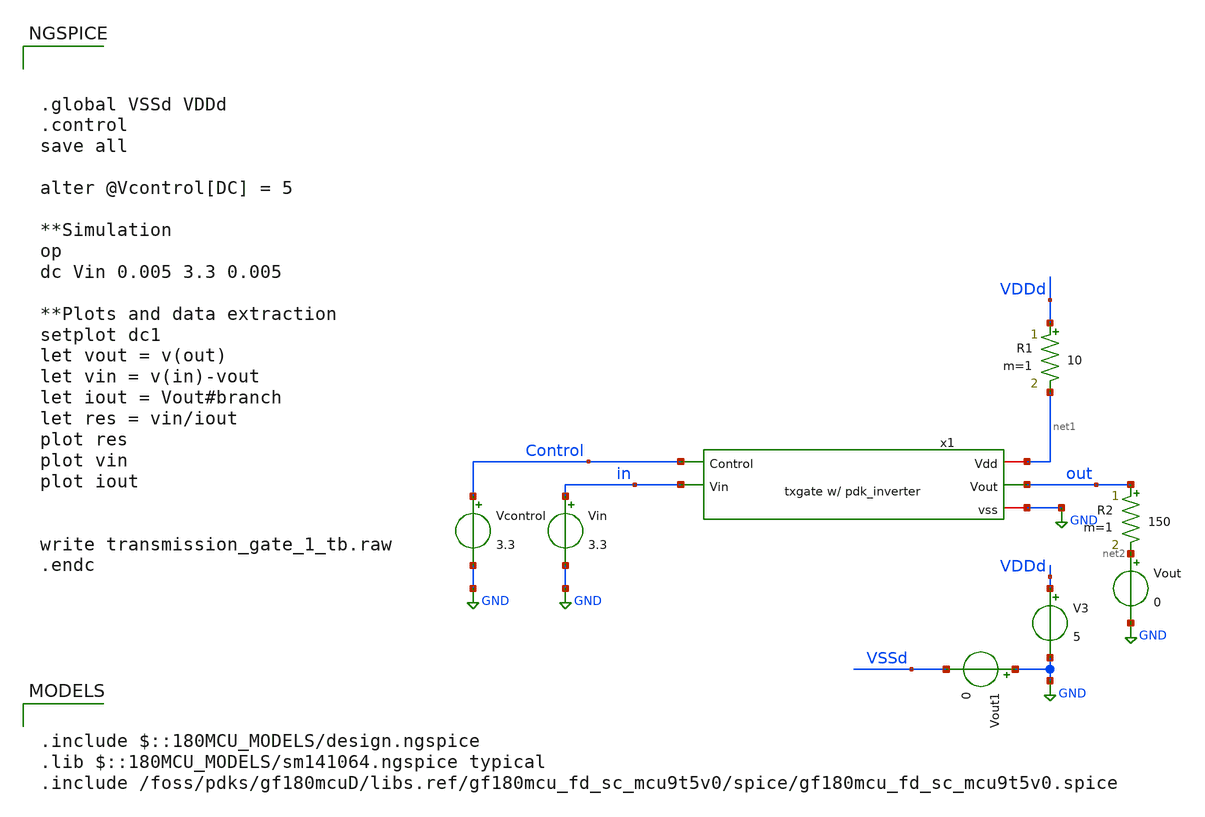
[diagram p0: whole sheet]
** sch_path: designs/libs/tb_analog/tb_txgate/transmission_gate_1_tb.sch
**.subckt transmission_gate_1_tb
Vin in GND 3.3
Vcontrol Control GND 3.3
V3 VDDd GND 5
Vout net2 GND 0
R1 VDDd net1 10 m=1
x1 net1 Control out in GND transmission_gate_2
Vout1 GND VSSd 0
R2 out net2 150 m=1
**** begin user architecture code

.include $::180MCU_MODELS/design.ngspice
.lib $::180MCU_MODELS/sm141064.ngspice typical
.include /foss/pdks/gf180mcuD/libs.ref/gf180mcu_fd_sc_mcu9t5v0/spice/gf180mcu_fd_sc_mcu9t5v0.spice




.global VSSd VDDd
.control
save all

alter @Vcontrol[DC] = 5

**Simulation
op
dc Vin 0.005 3.3 0.005

**Plots and data extraction
setplot dc1
let vout = v(out)
let vin = v(in)-vout
let iout = Vout#branch
let res = vin/iout
plot res
plot vin
plot iout


write transmission_gate_1_tb.raw
.endc


**** end user architecture code
**.ends

* expanding   symbol:  libs/core_analog/tx_gate/transmission_gate_2.sym # of pins=5
** sym_path: designs/libs/core_analog/tx_gate/transmission_gate_2.sym
** sch_path: designs/libs/core_analog/tx_gate/transmission_gate_2.sch
.subckt transmission_gate_2 Vdd Control Vout Vin vss
*.iopin Vdd
*.ipin Control
*.opin Vout
*.ipin Vin
*.iopin vss
XM3 Vout Control Vin vss nfet_03v3 L=0.28u W=6u nf=1 ad='int((nf+1)/2) * W/nf * 0.18u' as='int((nf+2)/2) * W/nf * 0.18u'
+ pd='2*int((nf+1)/2) * (W/nf + 0.18u)' ps='2*int((nf+2)/2) * (W/nf + 0.18u)' nrd='0.18u / W' nrs='0.18u / W'
+ sa=0 sb=0 sd=0 m=4
XM4 Vout net1 Vin Vdd pfet_03v3 L=0.28u W=6u nf=1 ad='int((nf+1)/2) * W/nf * 0.18u' as='int((nf+2)/2) * W/nf * 0.18u'
+ pd='2*int((nf+1)/2) * (W/nf + 0.18u)' ps='2*int((nf+2)/2) * (W/nf + 0.18u)' nrd='0.18u / W' nrs='0.18u / W'
+ sa=0 sb=0 sd=0 m=12
x1 Control VSSd VDDd VSSd VDDd net1 gf180mcu_fd_sc_mcu9t5v0__inv_1
**** begin user architecture code

.include $::180MCU_MODELS/design.ngspice
.include /foss/pdks/gf180mcuD/libs.ref/gf180mcu_fd_sc_mcu9t5v0/spice/gf180mcu_fd_sc_mcu9t5v0.spice
.lib $::180MCU_MODELS/sm141064.ngspice typical

**** end user architecture code
.ends

.GLOBAL GND
.end
